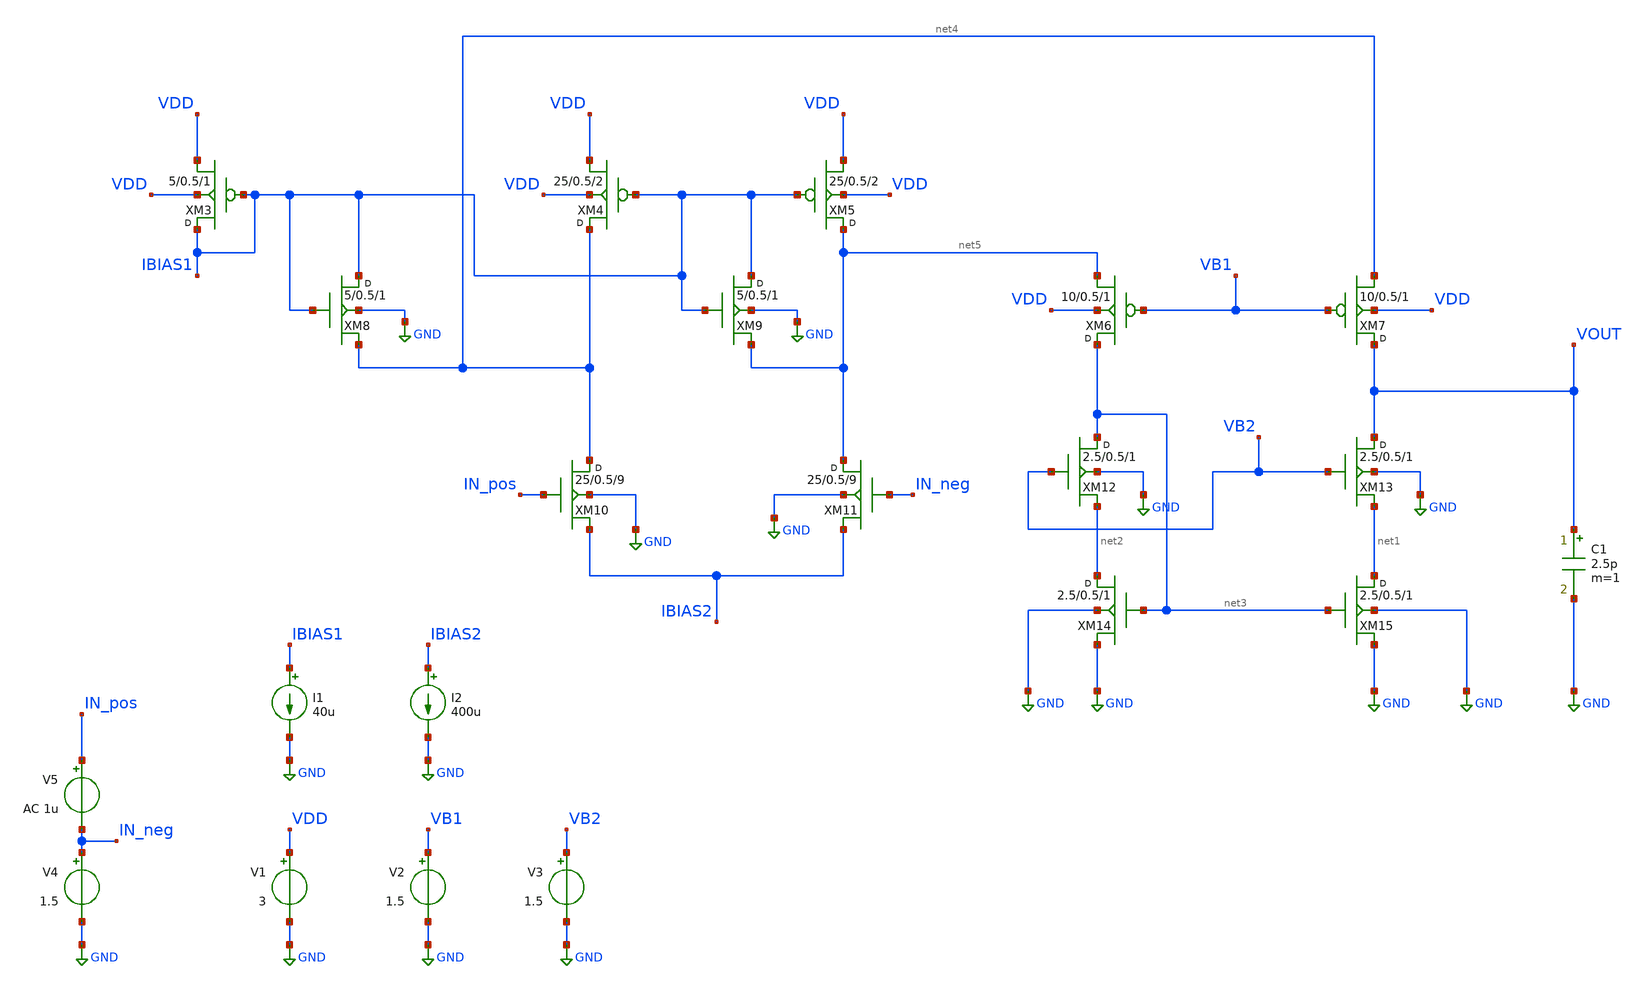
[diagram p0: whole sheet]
** sch_path: Designs/Comparator/Schematic/comparator.sch
**.subckt comparator
XM3 IBIAS1 IBIAS1 VDD VDD sky130_fd_pr__pfet_g5v0d10v5 w=5 l=0.5 m=1
XM4 net4 IBIAS1 VDD VDD sky130_fd_pr__pfet_g5v0d10v5 w=25 l=0.5 m=2
XM5 net5 IBIAS1 VDD VDD sky130_fd_pr__pfet_g5v0d10v5 w=25 l=0.5 m=2
XM6 net3 VB1 net5 VDD sky130_fd_pr__pfet_g5v0d10v5 w=10 l=0.5 m=1
XM7 VOUT VB1 net4 VDD sky130_fd_pr__pfet_g5v0d10v5 w=10 l=0.5 m=1
XM8 IBIAS1 IBIAS1 net4 GND sky130_fd_pr__nfet_g5v0d10v5 w=5 l=0.5 m=1
XM9 IBIAS1 IBIAS1 net5 GND sky130_fd_pr__nfet_g5v0d10v5 w=5 l=0.5 m=1
XM10 net4 IN_pos IBIAS2 GND sky130_fd_pr__nfet_g5v0d10v5 w=25 l=0.5 m=9
XM11 net5 IN_neg IBIAS2 GND sky130_fd_pr__nfet_g5v0d10v5 w=25 l=0.5 m=9
XM12 net3 VB2 net2 GND sky130_fd_pr__nfet_g5v0d10v5 w=2.5 l=0.5 m=1
XM13 VOUT VB2 net1 GND sky130_fd_pr__nfet_g5v0d10v5 w=2.5 l=0.5 m=1
XM14 net2 net3 GND GND sky130_fd_pr__nfet_g5v0d10v5 w=2.5 l=0.5 m=1
XM15 net1 net3 GND GND sky130_fd_pr__nfet_g5v0d10v5 w=2.5 l=0.5 m=1
I1 IBIAS1 GND 40u
I2 IBIAS2 GND 400u
V1 VDD GND 3
V2 VB1 GND 1.5
V3 VB2 GND 1.5
C1 VOUT GND 2.5p m=1
V4 IN_neg GND 1.5
V5 IN_pos IN_neg AC 1u
**** begin user architecture code

.include $::SKYWATER_MODELS/cells/nfet_01v8/sky130_fd_pr__nfet_01v8__tt.corner.spice
.include $::SKYWATER_MODELS/cells/nfet_01v8_lvt/sky130_fd_pr__nfet_01v8_lvt__tt.corner.spice
.include $::SKYWATER_MODELS/cells/pfet_01v8/sky130_fd_pr__pfet_01v8__tt.corner.spice
.include $::SKYWATER_MODELS/cells/nfet_03v3_nvt/sky130_fd_pr__nfet_03v3_nvt__tt.corner.spice
.include $::SKYWATER_MODELS/cells/nfet_05v0_nvt/sky130_fd_pr__nfet_05v0_nvt__tt.corner.spice
.include $::SKYWATER_MODELS/cells/esd_nfet_01v8/sky130_fd_pr__esd_nfet_01v8__tt.corner.spice
.include $::SKYWATER_MODELS/cells/pfet_01v8_lvt/sky130_fd_pr__pfet_01v8_lvt__tt.corner.spice
.include $::SKYWATER_MODELS/cells/pfet_01v8_hvt/sky130_fd_pr__pfet_01v8_hvt__tt.corner.spice
.include $::SKYWATER_MODELS/cells/esd_pfet_g5v0d10v5/sky130_fd_pr__esd_pfet_g5v0d10v5__tt.corner.spice
.include $::SKYWATER_MODELS/cells/pfet_g5v0d10v5/sky130_fd_pr__pfet_g5v0d10v5__tt.corner.spice
.include $::SKYWATER_MODELS/cells/pfet_g5v0d16v0/sky130_fd_pr__pfet_g5v0d16v0__tt.corner.spice
.include $::SKYWATER_MODELS/cells/nfet_g5v0d10v5/sky130_fd_pr__nfet_g5v0d10v5__tt.corner.spice
.include $::SKYWATER_MODELS/cells/nfet_g5v0d16v0/sky130_fd_pr__nfet_g5v0d16v0__tt_discrete.corner.spice
.include $::SKYWATER_MODELS/cells/esd_nfet_g5v0d10v5/sky130_fd_pr__esd_nfet_g5v0d10v5__tt.corner.spice
.include $::SKYWATER_MODELS/models/corners/tt/nonfet.spice
* Mismatch parameters
.include $::SKYWATER_MODELS/cells/nfet_01v8/sky130_fd_pr__nfet_01v8__mismatch.corner.spice
.include $::SKYWATER_MODELS/cells/pfet_01v8/sky130_fd_pr__pfet_01v8__mismatch.corner.spice
.include $::SKYWATER_MODELS/cells/nfet_01v8_lvt/sky130_fd_pr__nfet_01v8_lvt__mismatch.corner.spice
.include $::SKYWATER_MODELS/cells/pfet_01v8_lvt/sky130_fd_pr__pfet_01v8_lvt__mismatch.corner.spice
.include $::SKYWATER_MODELS/cells/pfet_01v8_hvt/sky130_fd_pr__pfet_01v8_hvt__mismatch.corner.spice
.include $::SKYWATER_MODELS/cells/nfet_g5v0d10v5/sky130_fd_pr__nfet_g5v0d10v5__mismatch.corner.spice
.include $::SKYWATER_MODELS/cells/pfet_g5v0d10v5/sky130_fd_pr__pfet_g5v0d10v5__mismatch.corner.spice
.include $::SKYWATER_MODELS/cells/nfet_05v0_nvt/sky130_fd_pr__nfet_05v0_nvt__mismatch.corner.spice
.include $::SKYWATER_MODELS/cells/nfet_03v3_nvt/sky130_fd_pr__nfet_03v3_nvt__mismatch.corner.spice
* Resistor$::SKYWATER_MODELS/Capacitor
.include $::SKYWATER_MODELS/models/r+c/res_typical__cap_typical.spice
.include $::SKYWATER_MODELS/models/r+c/res_typical__cap_typical__lin.spice
* Special cells
.include $::SKYWATER_MODELS/models/corners/tt/specialized_cells.spice
* All models
.include $::SKYWATER_MODELS/models/all.spice
* Corner
.include $::SKYWATER_MODELS/models/corners/tt/rf.spice
.include ~/skywater-pdk/libraries/sky130_fd_sc_hd/latest/cells/nand3/sky130_fd_sc_hd__nand3_1.spice
.include ~/skywater-pdk/libraries/sky130_fd_sc_hd/latest/cells/nand2/sky130_fd_sc_hd__nand2_1.spice
.include ~/skywater-pdk/libraries/sky130_fd_sc_hd/latest/cells/nor3/sky130_fd_sc_hd__nor3_1.spice
.include ~/skywater-pdk/libraries/sky130_fd_sc_hd/latest/cells/dfrtp/sky130_fd_sc_hd__dfrtp_1.spice
.include ~/skywater-pdk/libraries/sky130_fd_sc_hd/latest/cells/nor2/sky130_fd_sc_hd__nor2_1.spice
.include ~/skywater-pdk/libraries/sky130_fd_sc_hd/latest/cells/dlrbn/sky130_fd_sc_hd__dlrbn_1.spice
.include ~/skywater-pdk/libraries/sky130_fd_sc_hd/latest/cells/a31o/sky130_fd_sc_hd__a31o_2.spice
.include ~/skywater-pdk/libraries/sky130_fd_sc_hd/latest/cells/inv/sky130_fd_sc_hd__inv_1.spice
.include ~/skywater-pdk/libraries/sky130_fd_sc_hd/latest/cells/a222oi/sky130_fd_sc_hd__a222oi_1.spice
.include ~/skywater-pdk/libraries/sky130_fd_sc_hd/latest/cells/or2/sky130_fd_sc_hd__or2_1.spice
.include ~/skywater-pdk/libraries/sky130_fd_sc_hd/latest/cells/o221ai/sky130_fd_sc_hd__o221ai_1.spice




.options filetype=ascii
.ac dec 100 10 100Meg
.save all

**** end user architecture code
**.ends
.GLOBAL GND
.end
